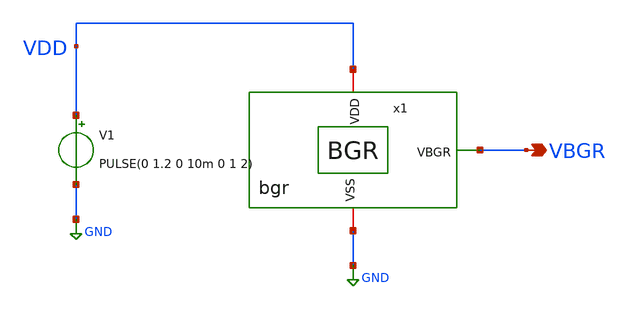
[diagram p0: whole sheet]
** sch_path: schematic/bgr/bgr_tb.sch
**.subckt bgr_tb VBGR
*.opin VBGR
V1 VDD GND PULSE(0 1.2 0 10m 0 1 2)
x1 VBGR VDD GND bgr
**** begin user architecture code

.lib $::SG13G2_MODELS/cornerCAP.lib cap_typ
.lib $::SG13G2_MODELS/cornerRES.lib res_typ
.lib cornerMOSlv.lib mos_tt
*.lib /foss/pdks/ihp-sg13g2/libs.tech/ngspice/models/cornerCAP.lib cap_typ
*.lib /foss/pdks/ihp-sg13g2/libs.tech/ngspice/models/cornerRES.lib res_typ
*.lib /foss/pdks/ihp-sg13g2/libs.tech/ngspice/models/cornerMOSlv.lib mos_tt



.option rshunt=1.0e12
.control
save all
save VDD
alter V1 dc 1.2

op
print I(Vmeas)

dc TEMP 100 -50 -5
print I(Vmeas)

write bgr_temp.raw
.endc

.control
save all
tran 1u 15m

print I(Vmeas)

write bandgap_transient.raw
.endc



**** end user architecture code
**.ends
.GLOBAL GND
.end
